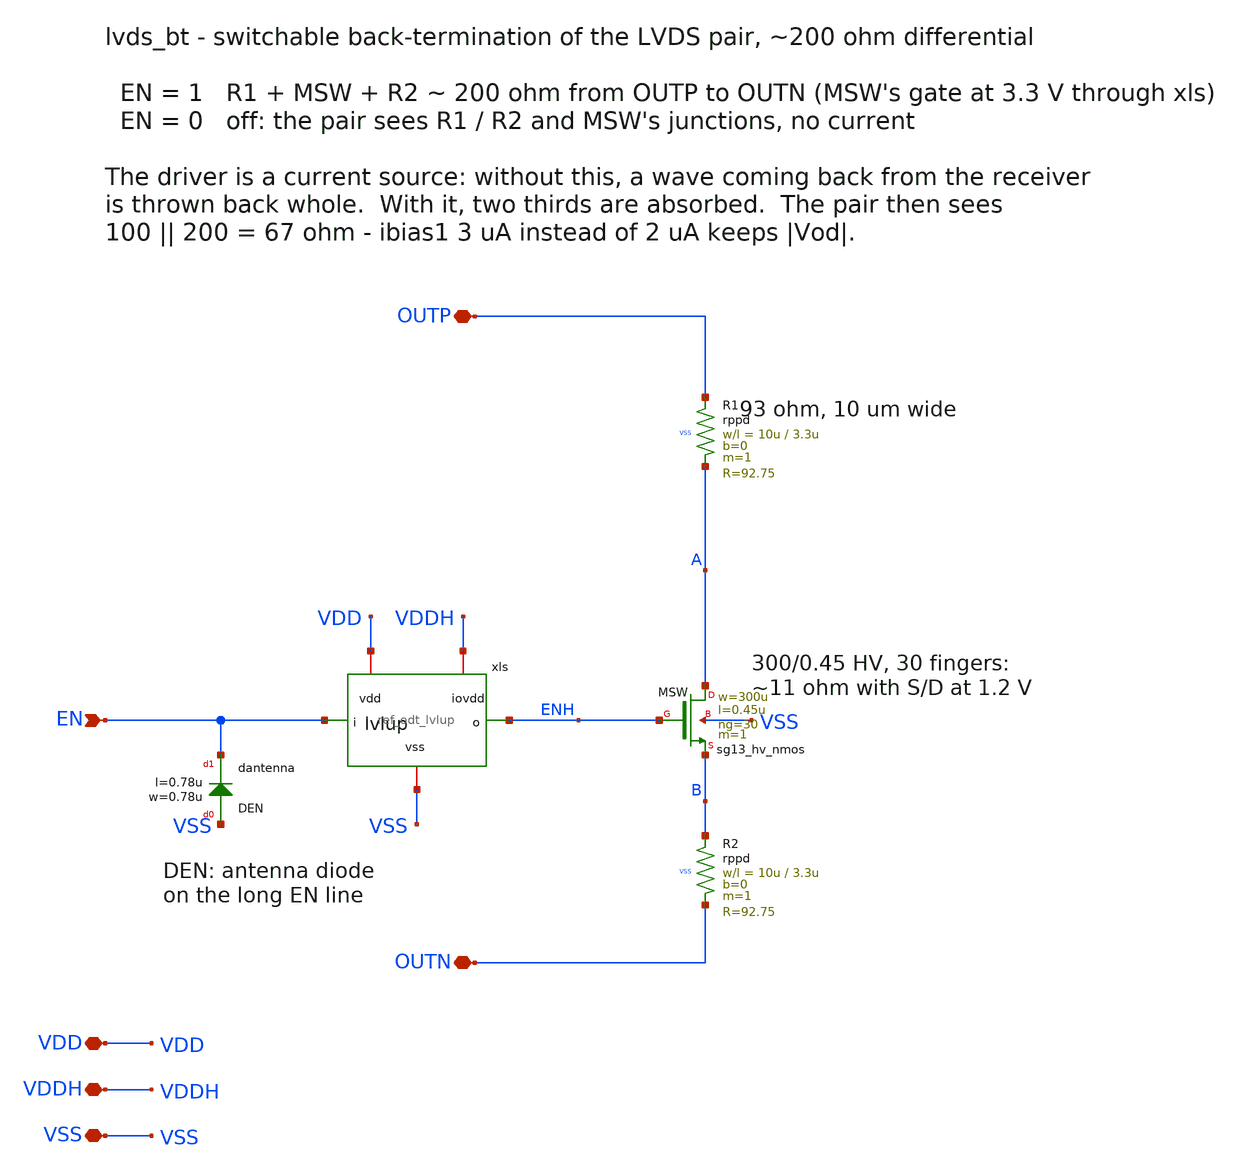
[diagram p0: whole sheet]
** sch_path: macros/lvds_bt/schematic/xschem/lvds_bt.sch
**.subckt lvds_bt OUTP OUTN EN VDD VDDH VSS
*.iopin OUTP
*.iopin OUTN
*.ipin EN
*.iopin VDD
*.iopin VDDH
*.iopin VSS
XR1 OUTP A VSS rppd w=10u l=3.3u m=1 b=0 mm_ok=1
XMSW A ENH B VSS sg13_hv_nmos w=300u l=0.45u ng=30 m=1 mm_ok=1
XR2 B OUTN VSS rppd w=10u l=3.3u m=1 b=0 mm_ok=1
xls EN ENH VDD VDDH VSS ref_odt_lvlup
XDEN VSS EN dantenna l=0.78u w=0.78u
**.ends

* expanding   symbol:  ref_odt_lvlup.sym # of pins=5
** sym_path: macros/ref_odt/schematic/xschem/ref_odt_lvlup.sym
** sch_path: macros/ref_odt/schematic/xschem/ref_odt_lvlup.sch
.subckt ref_odt_lvlup i o vdd iovdd vss
*.ipin i
*.opin o
*.iopin vdd
*.iopin iovdd
*.iopin vss
XMP_I IN_N i vdd vdd sg13_lv_pmos w=4.75u l=0.13u ng=1 m=1 mm_ok=1
XMN_I IN_N i vss vss sg13_lv_nmos w=2.75u l=0.13u ng=1 m=1 mm_ok=1
XMP_LN LVLD_N LVLD iovdd iovdd sg13_hv_pmos w=0.3u l=0.45u ng=1 m=1 mm_ok=1
XMN_LN LVLD_N i vss vss sg13_hv_nmos w=1.9u l=0.45u ng=1 m=1 mm_ok=1
XMP_L LVLD LVLD_N iovdd iovdd sg13_hv_pmos w=0.3u l=0.45u ng=1 m=1 mm_ok=1
XMN_L LVLD IN_N vss vss sg13_hv_nmos w=1.9u l=0.45u ng=1 m=1 mm_ok=1
XMP_O o LVLD_N iovdd iovdd sg13_hv_pmos w=3.9u l=0.45u ng=1 m=1 mm_ok=1
XMN_O o LVLD_N vss vss sg13_hv_nmos w=1.9u l=0.45u ng=1 m=1 mm_ok=1
.ends

.end
